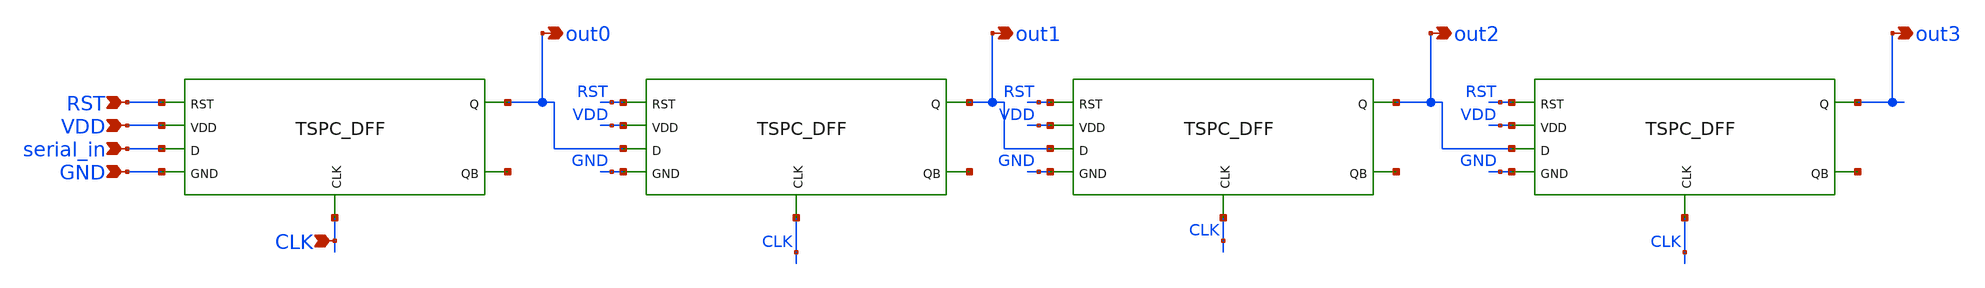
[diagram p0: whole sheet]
** sch_path: blocks/dsp-fft/sch/shift_reg.sch
**.subckt shift_reg VDD RST GND CLK out0 out1 out2 out3 serial_in
*.ipin VDD
*.ipin RST
*.ipin GND
*.ipin CLK
*.opin out0
*.opin out1
*.opin out2
*.opin out3
*.ipin serial_in
x1 RST VDD CLK serial_in net1 out0 GND tspc_dff
x2 RST VDD CLK out0 net2 out1 GND tspc_dff
x3 RST VDD CLK out1 net3 out2 GND tspc_dff
x4 RST VDD CLK out2 net4 out3 GND tspc_dff
**.ends
.end
